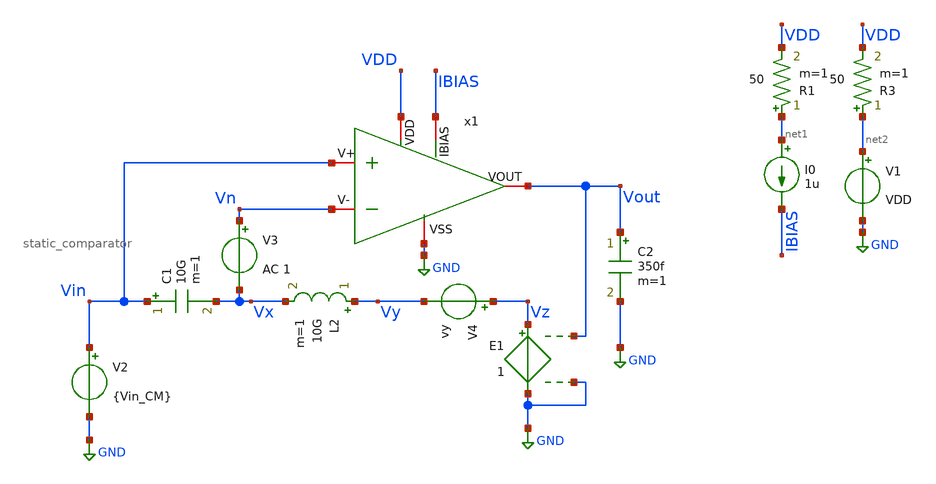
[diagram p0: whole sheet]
** sch_path: designs/static_comparator/xschem/static_comparator_tb.sch
**.subckt static_comparator_tb
x1 VDD IBIAS GND Vin Vn Vout static_comparator
I0 net1 IBIAS 1u
V1 net2 GND VDD
V2 Vin GND {Vin_CM}
V3 Vn Vx AC 1
C1 Vin Vx 10G m=1
L2 Vy Vx 10G m=1
E1 Vz GND Vout GND 1
C2 Vout GND 350f m=1
V4 Vz Vy vy
R3 net2 VDD 50 m=1
R1 net1 VDD 50 m=1
**** begin user architecture code




* --- Include PDK and Model Files ---
.include /foss/pdks/gf180mcuD/libs.tech/ngspice/design.ngspice
.lib /foss/pdks/gf180mcuD/libs.tech/ngspice/sm141064.ngspice typical

* --- Define Parameters for the Simulation ---
.param VDD = 1.8
.param VSS = 0
.param Vin_CM = 1
.param Vout_CM = 0.9
.param Vy = (Vout_CM - Vin_CM)
.param load_cap = 350*1e-15

* --- Simulation Commands and Analysis ---


*+ abstol=1e-14 savecurrents
.control
    save all

** OP simulation
op

** All OP parameters

let #####_M1_nmos_input_##### = 0
let id_M1 = @m.x1.xm1.m0[id]
let gm_M1 = @m.x1.xm1.m0[gm]
let ro_M1 = 1/@m.x1.xm1.m0[gds]
let Vsg_M1 = @m.x1.xm1.m0[vgs]
let Vsd_M1 = @m.x1.xm1.m0[vds]
let Vbs_M1 = -@m.x1.xm1.m0[vbs]
let Vdsat_M1 = @m.x1.xm1.m0[vdsat]
let Vth_M1 = @m.x1.xm1.m0[vth]
let ao_M1 = gm_M1*ro_M1
let gmid_M1 = gm_M1/id_M1
let fT_M1 = gm_M1/(6.283185*@m.x1.xm1.m0[cgg])
print #####_M1_nmos_input_##### id_M1 gm_M1 ro_M1 Vsg_M1 Vsd_M1 Vbs_M1 Vdsat_M1 Vth_M1 ao_M1 gmid_M1
+ fT_M1

let #####_M2_nmos_current_##### = 0
let id_M2 = @m.x1.xm2.m0[id]
let gm_M2 = @m.x1.xm2.m0[gm]
let ro_M2 = 1/@m.x1.xm2.m0[gds]
let Vsg_M2 = @m.x1.xm2.m0[vgs]
let Vsd_M2 = @m.x1.xm2.m0[vds]
let Vbs_M2 = -@m.x1.xm2.m0[vbs]
let Vdsat_M2 = @m.x1.xm2.m0[vdsat]
let Vth_M2 = @m.x1.xm2.m0[vth]
let ao_M2 = gm_M2*ro_M2
let gmid_M2 = gm_M2/id_M2
let fT_M2 = gm_M2/(6.283185*@m.x1.xm2.m0[cgg])
print #####_M2_nmos_current_##### id_M2 gm_M2 ro_M2 Vsg_M2 Vsd_M2 Vbs_M2 Vdsat_M2 Vth_M2 ao_M2
+ gmid_M2 fT_M2

let #####_M3_pmos_current_top_##### = 0
let id_M3 = @m.x1.xm3.m0[id]
let gm_M3 = @m.x1.xm3.m0[gm]
let ro_M3 = 1/@m.x1.xm3.m0[gds]
let Vsg_M3 = @m.x1.xm3.m0[vgs]
let Vsd_M3 = @m.x1.xm3.m0[vds]
let Vbs_M3 = -@m.x1.xm3.m0[vbs]
let Vdsat_M3 = @m.x1.xm3.m0[vdsat]
let Vth_M3 = @m.x1.xm3.m0[vth]
let ao_M3 = gm_M3*ro_M3
let gmid_M3 = gm_M3/id_M3
let fT_M3 = gm_M3/(6.283185*@m.x1.xm3.m0[cgg])
print #####_M3_pmos_current_top_##### id_M3 gm_M3 ro_M3 Vsg_M3 Vsd_M3 Vbs_M3 Vdsat_M3 Vth_M3 ao_M3
+ gmid_M3 fT_M3

let #####_M4_pmos_top_##### = 0
let id_M4 = @m.x1.xm4.m0[id]
let gm_M4 = @m.x1.xm4.m0[gm]
let ro_M4 = 1/@m.x1.xm4.m0[gds]
let Vsg_M4 = @m.x1.xm4.m0[vgs]
let Vsd_M4 = @m.x1.xm4.m0[vds]
let Vbs_M4 = -@m.x1.xm4.m0[vbs]
let Vdsat_M4 = @m.x1.xm4.m0[vdsat]
let Vth_M4 = @m.x1.xm4.m0[vth]
let ao_M4 = gm_M4*ro_M4
let gmid_M4 = gm_M4/id_M4
let fT_M4 = gm_M4/(6.283185*@m.x1.xm4.m0[cgg])
print #####_M4_pmos_top_##### id_M4 gm_M4 ro_M4 Vsg_M4 Vsd_M4 Vbs_M4 Vdsat_M4 Vth_M4 ao_M4 gmid_M4
+ fT_M4

let #####_M5_pmos_vp_##### = 0
let id_M5 = @m.x1.xm5.m0[id]
let gm_M5 = @m.x1.xm5.m0[gm]
let ro_M5 = 1/@m.x1.xm5.m0[gds]
let Vsg_M5 = @m.x1.xm5.m0[vgs]
let Vsd_M5 = @m.x1.xm5.m0[vds]
let Vbs_M5 = -@m.x1.xm5.m0[vbs]
let Vdsat_M5 = @m.x1.xm5.m0[vdsat]
let Vth_M5 = @m.x1.xm5.m0[vth]
let ao_M5 = gm_M5*ro_M5
let gmid_M5 = gm_M5/id_M5
let fT_M5 = gm_M5/(6.283185*@m.x1.xm5.m0[cgg])
print #####_M5_pmos_vp_##### id_M5 gm_M5 ro_M5 Vsg_M5 Vsd_M5 Vbs_M5 Vdsat_M5 Vth_M5 ao_M5 gmid_M5
+ fT_M5

let #####_M6_pmos_vn_##### = 0
let id_M6 = @m.x1.xm6.m0[id]
let gm_M6 = @m.x1.xm6.m0[gm]
let ro_M6 = 1/@m.x1.xm6.m0[gds]
let Vsg_M6 = @m.x1.xm6.m0[vgs]
let Vsd_M6 = @m.x1.xm6.m0[vds]
let Vbs_M6 = -@m.x1.xm6.m0[vbs]
let Vdsat_M6 = @m.x1.xm6.m0[vdsat]
let Vth_M6 = @m.x1.xm6.m0[vth]
let ao_M6 = gm_M6*ro_M6
let gmid_M6 = gm_M6/id_M6
let fT_M6 = gm_M6/(6.283185*@m.x1.xm6.m0[cgg])
print #####_M6_pmos_vn_##### id_M6 gm_M6 ro_M6 Vsg_M6 Vsd_M6 Vbs_M6 Vdsat_M6 Vth_M6 ao_M6 gmid_M6
+ fT_M6

let #####_M7_nmos_vp_##### = 0
let id_M7 = @m.x1.xm7.m0[id]
let gm_M7 = @m.x1.xm7.m0[gm]
let ro_M7 = 1/@m.x1.xm7.m0[gds]
let Vgs_M7 = @m.x1.xm7.m0[vgs]
let Vds_M7 = @m.x1.xm7.m0[vds]
let Vsb_M7 = -@m.x1.xm7.m0[vbs]
let Vdsat_M7 = @m.x1.xm7.m0[vdsat]
let Vth_M7 = @m.x1.xm7.m0[vth]
let ao_M7 = gm_M7*ro_M7
let gmid_M7 = gm_M7/id_M7
let fT_M7 = gm_M7/(6.283185*@m.x1.xm7.m0[cgg])
print #####_M7_nmos_vp_##### id_M7 gm_M7 ro_M7 Vgs_M7 Vds_M7 Vsb_M7 Vdsat_M7 Vth_M7 ao_M7 gmid_M7
+ fT_M7

let #####_M8_nmos_vn_##### = 0
let id_M8 = @m.x1.xm8.m0[id]
let gm_M8 = @m.x1.xm8.m0[gm]
let ro_M8 = 1/@m.x1.xm8.m0[gds]
let Vgs_M8 = @m.x1.xm8.m0[vgs]
let Vds_M8 = @m.x1.xm8.m0[vds]
let Vsb_M8 = -@m.x1.xm8.m0[vbs]
let Vdsat_M8 = @m.x1.xm8.m0[vdsat]
let Vth_M8 = @m.x1.xm8.m0[vth]
let ao_M8 = gm_M8*ro_M8
let gmid_M8 = gm_M8/id_M8
let fT_M8 = gm_M8/(6.283185*@m.x1.xm8.m0[cgg])
print #####_M8_nmos_vn_##### id_M8 gm_M8 ro_M8 Vgs_M8 Vds_M8 Vsb_M8 Vdsat_M8 Vth_M8 ao_M8 gmid_M8
+ fT_M8

let #####_M9_pmos_bottom_##### = 0
let id_M9 = @m.x1.xm9.m0[id]
let gm_M9 = @m.x1.xm9.m0[gm]
let ro_M9 = 1/@m.x1.xm9.m0[gds]
let Vgs_M9 = @m.x1.xm9.m0[vgs]
let Vds_M9 = @m.x1.xm9.m0[vds]
let Vsb_M9 = -@m.x1.xm9.m0[vbs]
let Vdsat_M9 = @m.x1.xm9.m0[vdsat]
let Vth_M9 = @m.x1.xm9.m0[vth]
let ao_M9 = gm_M9*ro_M9
let gmid_M9 = gm_M9/id_M9
let fT_M9 = gm_M9/(6.283185*@m.x1.xm9.m0[cgg])
print #####_M9_pmos_bottom_##### id_M9 gm_M9 ro_M9 Vgs_M9 Vds_M9 Vsb_M9 Vdsat_M9 Vth_M9 ao_M9
+ gmid_M9 fT_M9

let #####_M10_pmos_bottom_##### = 0
let id_M10 = @m.x1.xm10.m0[id]
let gm_M10 = @m.x1.xm10.m0[gm]
let ro_M10 = 1/@m.x1.xm10.m0[gds]
let Vgs_M10 = @m.x1.xm10.m0[vgs]
let Vds_M10 = @m.x1.xm10.m0[vds]
let Vsb_M10 = @m.x1.xm10.m0[vbs]
let Vdsat_M10 = @m.x1.xm10.m0[vdsat]
let Vth_M10 = @m.x1.xm10.m0[vth]
let ao_M10 = gm_M10*ro_M10
let gmid_M10 = gm_M10/id_M10
let fT_M10 = gm_M10/(6.283185*@m.x1.xm10.m0[cgg])
print #####_M10_pmos_bottom_##### id_M10 gm_M10 ro_M10 Vgs_M10 Vds_M10 Vsb_M10 Vdsat_M10 Vth_M10
+ ao_M10 gmid_M10 fT_M10

let #####_M11_nmos_voutn_##### = 0
let id_M11 = @m.x1.xm11.m0[id]
let gm_M11 = @m.x1.xm11.m0[gm]
let ro_M11 = 1/@m.x1.xm11.m0[gds]
let Vsg_M11 = @m.x1.xm11.m0[vgs]
let Vsd_M11 = @m.x1.xm11.m0[vds]
let Vbs_M11 = -@m.x1.xm11.m0[vbs]
let Vdsat_M11 = @m.x1.xm11.m0[vdsat]
let Vth_M11 = @m.x1.xm11.m0[vth]
let ao_M11 = gm_M11*ro_M11
let gmid_M11 = gm_M11/id_M11
let fT_M11 = gm_M11/(6.283185*@m.x1.xm11.m0[cgg])
print #####_M11_nmos_voutn_##### id_M11 gm_M11 ro_M11 Vsg_M11 Vsd_M11 Vbs_M11 Vdsat_M11 Vth_M11
+ ao_M11 gmid_M11 fT_M11

let #####_M12_nmos_voutp_##### = 0
let id_M12 = @m.x1.xm12.m0[id]
let gm_M12 = @m.x1.xm12.m0[gm]
let ro_M12 = 1/@m.x1.xm12.m0[gds]
let Vsg_M12 = @m.x1.xm12.m0[vgs]
let Vsd_M12 = @m.x1.xm12.m0[vds]
let Vbs_M12 = -@m.x1.xm12.m0[vbs]
let Vdsat_M12 = @m.x1.xm12.m0[vdsat]
let Vth_M12 = @m.x1.xm12.m0[vth]
let ao_M12 = gm_M12*ro_M12
let gmid_M12 = gm_M12/id_M12
let fT_M12 = gm_M12/(6.283185*@m.x1.xm12.m0[cgg])
print #####_M12_nmos_voutp_##### id_M12 gm_M12 ro_M12 Vsg_M12 Vsd_M12 Vbs_M12 Vdsat_M12 Vth_M12
+ ao_M12 gmid_M12 fT_M12


let #####_potencia_##### = 0
let Pwr = (id_M1 + id_M2 + id_M4 + id_M9 + id_M10)*1.8
print #####_potencia_##### Pwr

** Custom output
let #####_Custom_output_##### = 0

print #####_Custom_output_##### Av BW BW_2 Rout gm_M1 ro_M1 gm_M6 ro_M6 ro_M4 gm_M8 ro_M8 ro_M10


    remzerovec
    * write static_comparator_tb.raw
    set appendwrite

    * run ac simulation
    ac dec 20 1 100e7

    * measure parameters
    let vout_mag_VV = abs(v(Vout))
    let vout_mag = db(abs(v(Vout)))
    let vout_phase = cph(v(Vout)) * 180/pi
    let gm = (-1)*db(abs(v(Vout)))

    meas ac A0 find vout_mag at=1
    meas ac UGB when vout_mag=0 fall=1
    meas ac PM find vout_phase when vout_mag=0
    meas ac GM find gm when vout_phase=0

    let A0_p1 = A0 - 3
    meas ac BW when vout_mag=A0_p1

    *plot vout_mag
    *plot vout_phase

    write static_comparator_tb.raw
.endc



**** end user architecture code
**.ends

* expanding   symbol:  gf180/static_comparator/xschem/static_comparator.sym # of pins=6
** sym_path: gf180/static_comparator/xschem/static_comparator.sym
** sch_path: gf180/static_comparator/xschem/static_comparator.sch
.subckt static_comparator VDD IBIAS VSS V+ V- VOUT
*.iopin IBIAS
*.iopin VSS
*.iopin VDD
*.iopin V+
*.iopin V-
*.iopin VOUT
XM1 IBIAS IBIAS VSS VSS nfet_03v3 L=4u W=1.1u nf=1 ad='int((nf+1)/2) * W/nf * 0.18u' as='int((nf+2)/2) * W/nf * 0.18u'
+ pd='2*int((nf+1)/2) * (W/nf + 0.18u)' ps='2*int((nf+2)/2) * (W/nf + 0.18u)' nrd='0.18u / W' nrs='0.18u / W'
+ sa=0 sb=0 sd=0 m=1
XM3 net1 net1 VDD VDD pfet_03v3 L=2u W=4.5u nf=1 ad='int((nf+1)/2) * W/nf * 0.18u' as='int((nf+2)/2) * W/nf * 0.18u'
+ pd='2*int((nf+1)/2) * (W/nf + 0.18u)' ps='2*int((nf+2)/2) * (W/nf + 0.18u)' nrd='0.18u / W' nrs='0.18u / W'
+ sa=0 sb=0 sd=0 m=1
XM2 net1 IBIAS VSS VSS nfet_03v3 L=4u W=625n nf=1 ad='int((nf+1)/2) * W/nf * 0.18u' as='int((nf+2)/2) * W/nf * 0.18u'
+ pd='2*int((nf+1)/2) * (W/nf + 0.18u)' ps='2*int((nf+2)/2) * (W/nf + 0.18u)' nrd='0.18u / W' nrs='0.18u / W'
+ sa=0 sb=0 sd=0 m=1
XM4 net2 net1 VDD VDD pfet_03v3 L=2u W=25u nf=1 ad='int((nf+1)/2) * W/nf * 0.18u' as='int((nf+2)/2) * W/nf * 0.18u'
+ pd='2*int((nf+1)/2) * (W/nf + 0.18u)' ps='2*int((nf+2)/2) * (W/nf + 0.18u)' nrd='0.18u / W' nrs='0.18u / W'
+ sa=0 sb=0 sd=0 m=1
XM5 Vx+ V+ net2 VDD pfet_03v3 L=360n W=2u nf=1 ad='int((nf+1)/2) * W/nf * 0.18u' as='int((nf+2)/2) * W/nf * 0.18u'
+ pd='2*int((nf+1)/2) * (W/nf + 0.18u)' ps='2*int((nf+2)/2) * (W/nf + 0.18u)' nrd='0.18u / W' nrs='0.18u / W'
+ sa=0 sb=0 sd=0 m=10
XM7 Vx+ Vx+ VSS VSS nfet_03v3 L=2u W=985n nf=1 ad='int((nf+1)/2) * W/nf * 0.18u' as='int((nf+2)/2) * W/nf * 0.18u'
+ pd='2*int((nf+1)/2) * (W/nf + 0.18u)' ps='2*int((nf+2)/2) * (W/nf + 0.18u)' nrd='0.18u / W' nrs='0.18u / W'
+ sa=0 sb=0 sd=0 m=1
XM6 Vx- V- net2 VDD pfet_03v3 L=360n W=2u nf=1 ad='int((nf+1)/2) * W/nf * 0.18u' as='int((nf+2)/2) * W/nf * 0.18u'
+ pd='2*int((nf+1)/2) * (W/nf + 0.18u)' ps='2*int((nf+2)/2) * (W/nf + 0.18u)' nrd='0.18u / W' nrs='0.18u / W'
+ sa=0 sb=0 sd=0 m=10
XM8 Vx- Vx- VSS VSS nfet_03v3 L=2u W=985n nf=1 ad='int((nf+1)/2) * W/nf * 0.18u' as='int((nf+2)/2) * W/nf * 0.18u'
+ pd='2*int((nf+1)/2) * (W/nf + 0.18u)' ps='2*int((nf+2)/2) * (W/nf + 0.18u)' nrd='0.18u / W' nrs='0.18u / W'
+ sa=0 sb=0 sd=0 m=1
XM9 net3 net3 VDD VDD pfet_03v3 L=4u W=950n nf=1 ad='int((nf+1)/2) * W/nf * 0.18u' as='int((nf+2)/2) * W/nf * 0.18u'
+ pd='2*int((nf+1)/2) * (W/nf + 0.18u)' ps='2*int((nf+2)/2) * (W/nf + 0.18u)' nrd='0.18u / W' nrs='0.18u / W'
+ sa=0 sb=0 sd=0 m=1
XM10 VOUT net3 VDD VDD pfet_03v3 L=4u W=950n nf=1 ad='int((nf+1)/2) * W/nf * 0.18u' as='int((nf+2)/2) * W/nf * 0.18u'
+ pd='2*int((nf+1)/2) * (W/nf + 0.18u)' ps='2*int((nf+2)/2) * (W/nf + 0.18u)' nrd='0.18u / W' nrs='0.18u / W'
+ sa=0 sb=0 sd=0 m=1
XM11 net3 Vx- VSS VSS nfet_03v3 L=2u W=1.1u nf=1 ad='int((nf+1)/2) * W/nf * 0.18u' as='int((nf+2)/2) * W/nf * 0.18u'
+ pd='2*int((nf+1)/2) * (W/nf + 0.18u)' ps='2*int((nf+2)/2) * (W/nf + 0.18u)' nrd='0.18u / W' nrs='0.18u / W'
+ sa=0 sb=0 sd=0 m=1
XM12 VOUT Vx+ VSS VSS nfet_03v3 L=2u W=1.1u nf=1 ad='int((nf+1)/2) * W/nf * 0.18u' as='int((nf+2)/2) * W/nf * 0.18u'
+ pd='2*int((nf+1)/2) * (W/nf + 0.18u)' ps='2*int((nf+2)/2) * (W/nf + 0.18u)' nrd='0.18u / W' nrs='0.18u / W'
+ sa=0 sb=0 sd=0 m=1
.ends

.GLOBAL GND
.end
